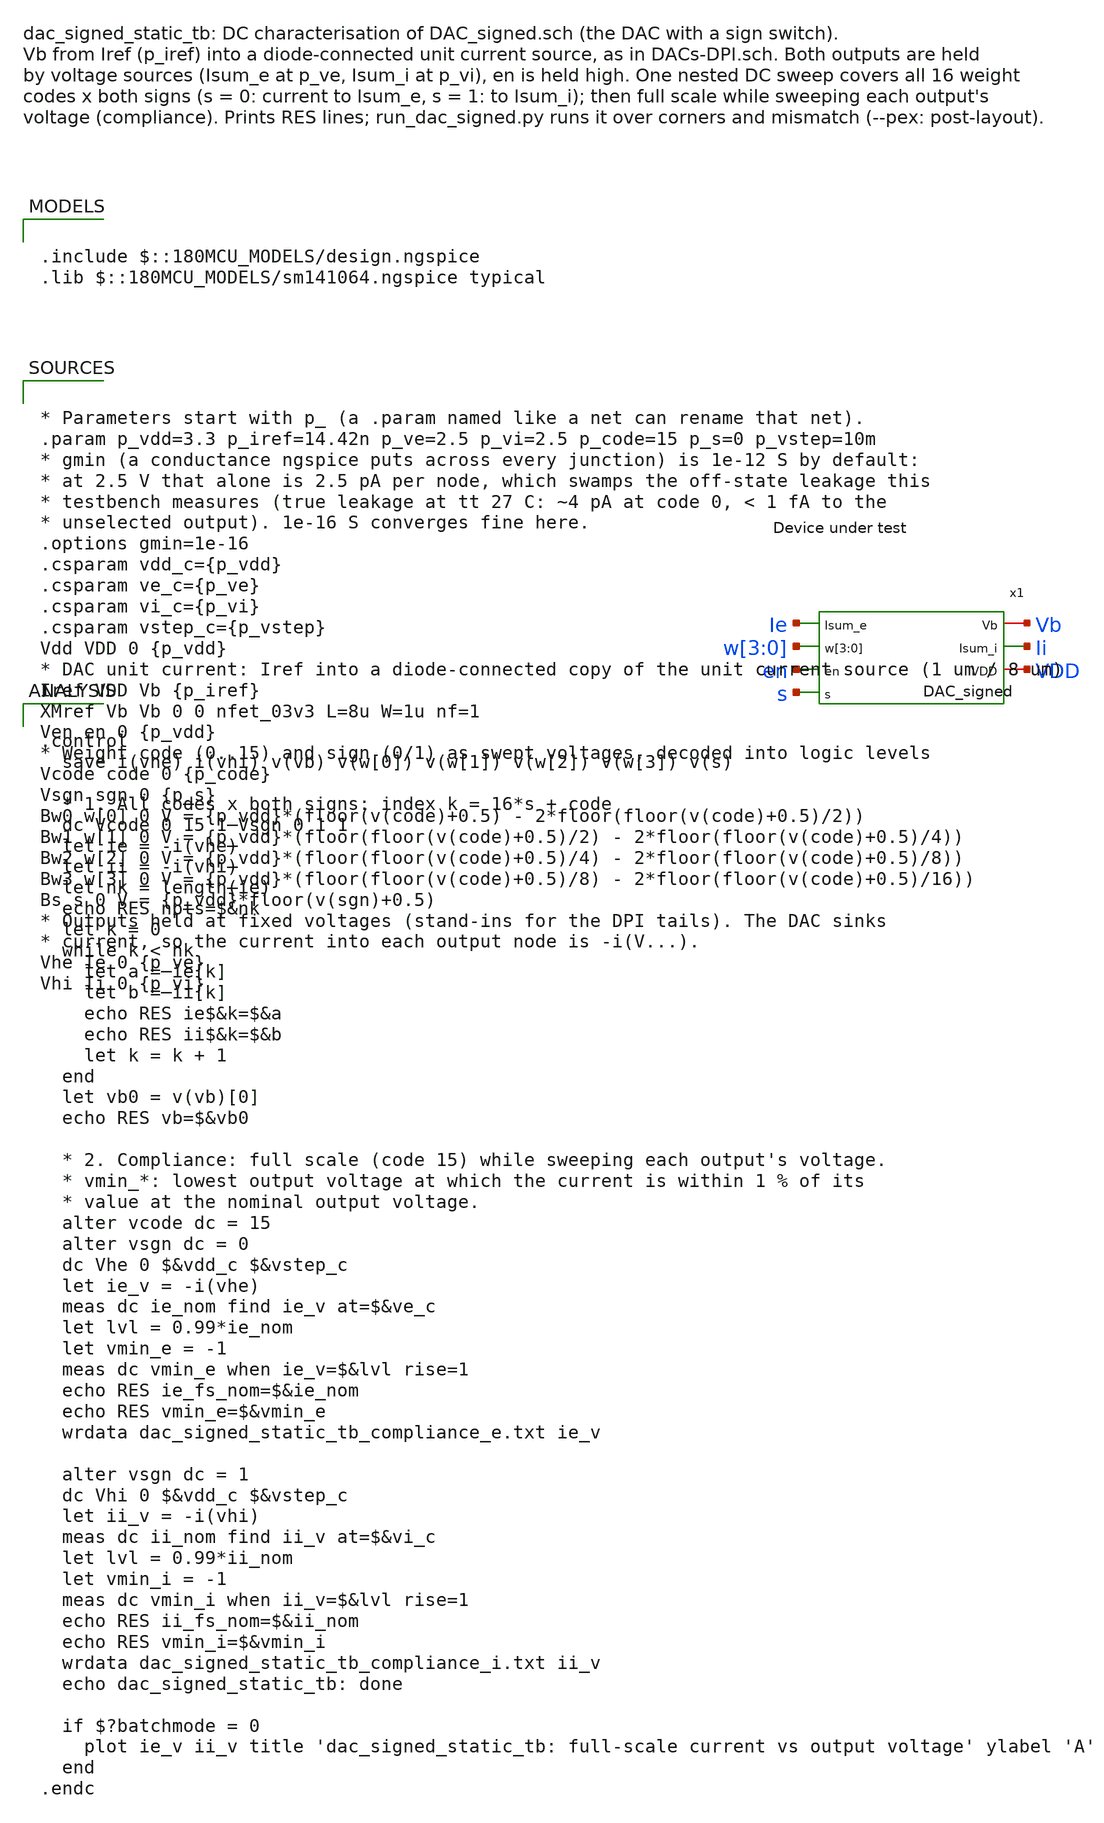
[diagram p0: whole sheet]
** sch_path: analog/testbenches/dac/dac_signed_static_tb.sch
**.subckt dac_signed_static_tb
x1 Ie w[3] w[2] w[1] w[0] en s Vb Ii VDD DAC_signed
**** begin user architecture code

.include $::180MCU_MODELS/design.ngspice
.lib $::180MCU_MODELS/sm141064.ngspice typical



* Parameters start with p_ (a .param named like a net can rename that net).
.param p_vdd=3.3 p_iref=14.42n p_ve=2.5 p_vi=2.5 p_code=15 p_s=0 p_vstep=10m
* gmin (a conductance ngspice puts across every junction) is 1e-12 S by default:
* at 2.5 V that alone is 2.5 pA per node, which swamps the off-state leakage this
* testbench measures (true leakage at tt 27 C: ~4 pA at code 0, < 1 fA to the
* unselected output). 1e-16 S converges fine here.
.options gmin=1e-16
.csparam vdd_c={p_vdd}
.csparam ve_c={p_ve}
.csparam vi_c={p_vi}
.csparam vstep_c={p_vstep}
Vdd VDD 0 {p_vdd}
* DAC unit current: Iref into a diode-connected copy of the unit current source (1 um / 8 um)
Iref VDD Vb {p_iref}
XMref Vb Vb 0 0 nfet_03v3 L=8u W=1u nf=1
Ven en 0 {p_vdd}
* Weight code (0..15) and sign (0/1) as swept voltages, decoded into logic levels
Vcode code 0 {p_code}
Vsgn sgn 0 {p_s}
Bw0 w[0] 0 V = {p_vdd}*(floor(v(code)+0.5) - 2*floor(floor(v(code)+0.5)/2))
Bw1 w[1] 0 V = {p_vdd}*(floor(floor(v(code)+0.5)/2) - 2*floor(floor(v(code)+0.5)/4))
Bw2 w[2] 0 V = {p_vdd}*(floor(floor(v(code)+0.5)/4) - 2*floor(floor(v(code)+0.5)/8))
Bw3 w[3] 0 V = {p_vdd}*(floor(floor(v(code)+0.5)/8) - 2*floor(floor(v(code)+0.5)/16))
Bs s 0 V = {p_vdd}*floor(v(sgn)+0.5)
* Outputs held at fixed voltages (stand-ins for the DPI tails). The DAC sinks
* current, so the current into each output node is -i(V...).
Vhe Ie 0 {p_ve}
Vhi Ii 0 {p_vi}




.control
  save i(vhe) i(vhi) v(vb) v(w[0]) v(w[1]) v(w[2]) v(w[3]) v(s)

  * 1. All codes x both signs: index k = 16*s + code
  dc Vcode 0 15 1 Vsgn 0 1 1
  let ie = -i(vhe)
  let ii = -i(vhi)
  let nk = length(ie)
  echo RES npts=$&nk
  let k = 0
  while k < nk
    let a = ie[k]
    let b = ii[k]
    echo RES ie$&k=$&a
    echo RES ii$&k=$&b
    let k = k + 1
  end
  let vb0 = v(vb)[0]
  echo RES vb=$&vb0

  * 2. Compliance: full scale (code 15) while sweeping each output's voltage.
  * vmin_*: lowest output voltage at which the current is within 1 % of its
  * value at the nominal output voltage.
  alter vcode dc = 15
  alter vsgn dc = 0
  dc Vhe 0 $&vdd_c $&vstep_c
  let ie_v = -i(vhe)
  meas dc ie_nom find ie_v at=$&ve_c
  let lvl = 0.99*ie_nom
  let vmin_e = -1
  meas dc vmin_e when ie_v=$&lvl rise=1
  echo RES ie_fs_nom=$&ie_nom
  echo RES vmin_e=$&vmin_e
  wrdata dac_signed_static_tb_compliance_e.txt ie_v

  alter vsgn dc = 1
  dc Vhi 0 $&vdd_c $&vstep_c
  let ii_v = -i(vhi)
  meas dc ii_nom find ii_v at=$&vi_c
  let lvl = 0.99*ii_nom
  let vmin_i = -1
  meas dc vmin_i when ii_v=$&lvl rise=1
  echo RES ii_fs_nom=$&ii_nom
  echo RES vmin_i=$&vmin_i
  wrdata dac_signed_static_tb_compliance_i.txt ii_v
  echo dac_signed_static_tb: done

  if $?batchmode = 0
    plot ie_v ii_v title 'dac_signed_static_tb: full-scale current vs output voltage' ylabel 'A'
  end
.endc


**** end user architecture code
**.ends

* expanding   symbol:  DAC_signed.sym # of pins=7
** sym_path: analog/neuron/DAC_signed.sym
** sch_path: analog/neuron/DAC_signed.sch
.subckt DAC_signed Isum_e w[3] w[2] w[1] w[0] en s Vb Isum_i VDD
*.ipin w[3],w[2],w[1],w[0]
*.ipin en
*.ipin s
*.iopin Vb
*.iopin VDD
*.iopin Isum_e
*.iopin Isum_i
x1 Y Vb w[3] w[2] w[1] w[0] en DAC
XMse Isum_e sb Y GND nfet_03v3 L=0.28u W=0.22u nf=1 ad='int((nf+1)/2) * W/nf * 0.18u' as='int((nf+2)/2)
+ * W/nf * 0.18u' pd='2*int((nf+1)/2) * (W/nf + 0.18u)' ps='2*int((nf+2)/2) * (W/nf + 0.18u)' nrd='0.18u
+ / W' nrs='0.18u / W' sa=0 sb=0 sd=0 m=1
XMsi Isum_i s Y GND nfet_03v3 L=0.28u W=0.22u nf=1 ad='int((nf+1)/2) * W/nf * 0.18u' as='int((nf+2)/2)
+ * W/nf * 0.18u' pd='2*int((nf+1)/2) * (W/nf + 0.18u)' ps='2*int((nf+2)/2) * (W/nf + 0.18u)' nrd='0.18u
+ / W' nrs='0.18u / W' sa=0 sb=0 sd=0 m=1
XMpi sb s VDD VDD pfet_03v3 L=0.28u W=0.44u nf=1 ad='int((nf+1)/2) * W/nf * 0.18u' as='int((nf+2)/2)
+ * W/nf * 0.18u' pd='2*int((nf+1)/2) * (W/nf + 0.18u)' ps='2*int((nf+2)/2) * (W/nf + 0.18u)' nrd='0.18u
+ / W' nrs='0.18u / W' sa=0 sb=0 sd=0 m=1
XMni sb s GND GND nfet_03v3 L=0.28u W=0.22u nf=1 ad='int((nf+1)/2) * W/nf * 0.18u' as='int((nf+2)/2)
+ * W/nf * 0.18u' pd='2*int((nf+1)/2) * (W/nf + 0.18u)' ps='2*int((nf+2)/2) * (W/nf + 0.18u)' nrd='0.18u
+ / W' nrs='0.18u / W' sa=0 sb=0 sd=0 m=1
.ends


* expanding   symbol:  DAC.sym # of pins=4
** sym_path: analog/neuron/DAC.sym
** sch_path: analog/neuron/DAC.sch
.subckt DAC Isum Vb w[3] w[2] w[1] w[0] en
*.iopin Vb
*.ipin w[3],w[2],w[1],w[0]
*.ipin Isum
*.ipin en
XM1 X w[0] net4 net4 nfet_03v3 L=0.28u W=0.22u nf=1 ad='int((nf+1)/2) * W/nf * 0.18u' as='int((nf+2)/2)
+ * W/nf * 0.18u' pd='2*int((nf+1)/2) * (W/nf + 0.18u)' ps='2*int((nf+2)/2) * (W/nf + 0.18u)' nrd='0.18u
+ / W' nrs='0.18u / W' sa=0 sb=0 sd=0 m=1
XM2 net4 Vb GND GND nfet_03v3 L=8u W=1u nf=1 ad='int((nf+1)/2) * W/nf * 0.18u' as='int((nf+2)/2) * W/nf
+ * 0.18u' pd='2*int((nf+1)/2) * (W/nf + 0.18u)' ps='2*int((nf+2)/2) * (W/nf + 0.18u)' nrd='0.18u / W' nrs='0.18u
+ / W' sa=0 sb=0 sd=0 m=1
XM3 X w[1] net2 net2 nfet_03v3 L=0.28u W=0.22u nf=1 ad='int((nf+1)/2) * W/nf * 0.18u' as='int((nf+2)/2)
+ * W/nf * 0.18u' pd='2*int((nf+1)/2) * (W/nf + 0.18u)' ps='2*int((nf+2)/2) * (W/nf + 0.18u)' nrd='0.18u
+ / W' nrs='0.18u / W' sa=0 sb=0 sd=0 m=2
XM4 net2 Vb GND GND nfet_03v3 L=8u W=1u nf=1 ad='int((nf+1)/2) * W/nf * 0.18u' as='int((nf+2)/2) * W/nf
+ * 0.18u' pd='2*int((nf+1)/2) * (W/nf + 0.18u)' ps='2*int((nf+2)/2) * (W/nf + 0.18u)' nrd='0.18u / W' nrs='0.18u
+ / W' sa=0 sb=0 sd=0 m=2
XM5 X w[2] net3 net3 nfet_03v3 L=0.28u W=0.22u nf=1 ad='int((nf+1)/2) * W/nf * 0.18u' as='int((nf+2)/2)
+ * W/nf * 0.18u' pd='2*int((nf+1)/2) * (W/nf + 0.18u)' ps='2*int((nf+2)/2) * (W/nf + 0.18u)' nrd='0.18u
+ / W' nrs='0.18u / W' sa=0 sb=0 sd=0 m=3
XM6 net3 Vb GND GND nfet_03v3 L=8u W=1u nf=1 ad='int((nf+1)/2) * W/nf * 0.18u' as='int((nf+2)/2) * W/nf
+ * 0.18u' pd='2*int((nf+1)/2) * (W/nf + 0.18u)' ps='2*int((nf+2)/2) * (W/nf + 0.18u)' nrd='0.18u / W' nrs='0.18u
+ / W' sa=0 sb=0 sd=0 m=3
XM7 X w[3] net1 net1 nfet_03v3 L=0.28u W=0.22u nf=1 ad='int((nf+1)/2) * W/nf * 0.18u' as='int((nf+2)/2)
+ * W/nf * 0.18u' pd='2*int((nf+1)/2) * (W/nf + 0.18u)' ps='2*int((nf+2)/2) * (W/nf + 0.18u)' nrd='0.18u
+ / W' nrs='0.18u / W' sa=0 sb=0 sd=0 m=4
XM8 net1 Vb GND GND nfet_03v3 L=8u W=1u nf=1 ad='int((nf+1)/2) * W/nf * 0.18u' as='int((nf+2)/2) * W/nf
+ * 0.18u' pd='2*int((nf+1)/2) * (W/nf + 0.18u)' ps='2*int((nf+2)/2) * (W/nf + 0.18u)' nrd='0.18u / W' nrs='0.18u
+ / W' sa=0 sb=0 sd=0 m=4
XMen Isum en X GND nfet_03v3 L=0.28u W=0.22u nf=1 ad='int((nf+1)/2) * W/nf * 0.18u' as='int((nf+2)/2)
+ * W/nf * 0.18u' pd='2*int((nf+1)/2) * (W/nf + 0.18u)' ps='2*int((nf+2)/2) * (W/nf + 0.18u)' nrd='0.18u
+ / W' nrs='0.18u / W' sa=0 sb=0 sd=0 m=1
.ends

.GLOBAL GND
.end
